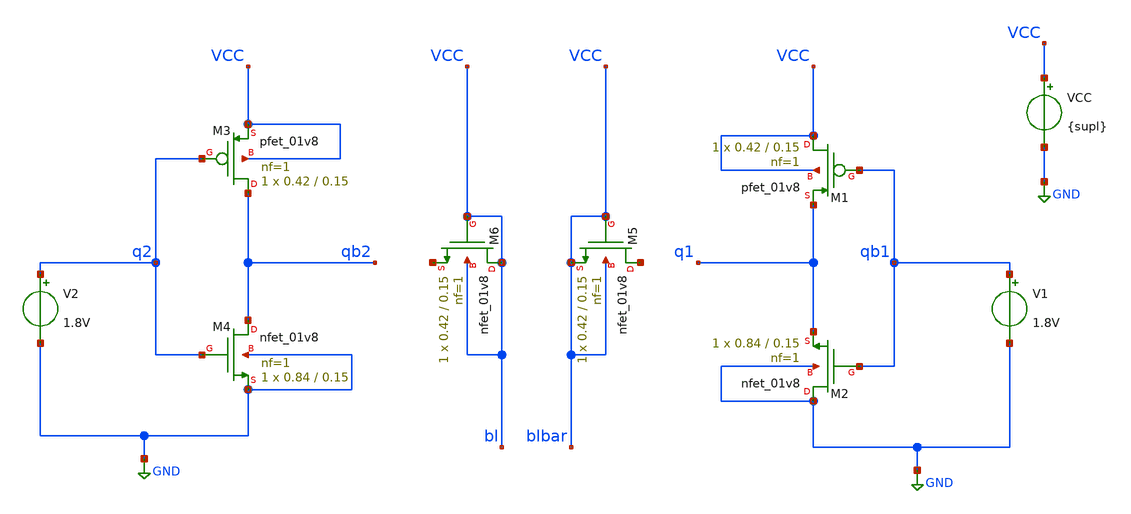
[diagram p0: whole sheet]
** sch_path: Schematics/holdsnm.sch
**.subckt holdsnm
XM1 VCC qb1 q1 VCC sky130_fd_pr__pfet_01v8 L=0.15 W=0.42 nf=1 ad='int((1 + 1)/2) * 0.42 / 1 * 0.29' as='int((1 + 2)/2) * 0.42 / 1 * 0.29'
+ pd='2*int((1 + 1)/2) * (0.42 / 1 + 0.29)' ps='2*int((1 + 2)/2) * (0.42 / 1 + 0.29)' nrd='0.29 / 0.42 '
+ nrs='0.29 / 0.42 ' sa=0 sb=0 sd=0 mult=1 m=1
XM2 GND qb1 q1 GND sky130_fd_pr__nfet_01v8 L=0.15 W=0.84 nf=1 ad='int((1 + 1)/2) * 0.84 / 1 * 0.29' as='int((1 + 2)/2) * 0.84 / 1 * 0.29'
+ pd='2*int((1 + 1)/2) * (0.84 / 1 + 0.29)' ps='2*int((1 + 2)/2) * (0.84 / 1 + 0.29)' nrd='0.29 / 0.84 '
+ nrs='0.29 / 0.84 ' sa=0 sb=0 sd=0 mult=1 m=1
XM3 qb2 q2 VCC VCC sky130_fd_pr__pfet_01v8 L=0.15 W=0.42 nf=1 ad='int((1 + 1)/2) * 0.42 / 1 * 0.29' as='int((1 + 2)/2) * 0.42 / 1 * 0.29'
+ pd='2*int((1 + 1)/2) * (0.42 / 1 + 0.29)' ps='2*int((1 + 2)/2) * (0.42 / 1 + 0.29)' nrd='0.29 / 0.42 '
+ nrs='0.29 / 0.42 ' sa=0 sb=0 sd=0 mult=1 m=1
XM4 qb2 q2 GND GND sky130_fd_pr__nfet_01v8 L=0.15 W=0.84 nf=1 ad='int((1 + 1)/2) * 0.84 / 1 * 0.29' as='int((1 + 2)/2) * 0.84 / 1 * 0.29'
+ pd='2*int((1 + 1)/2) * (0.84 / 1 + 0.29)' ps='2*int((1 + 2)/2) * (0.84 / 1 + 0.29)' nrd='0.29 / 0.84 '
+ nrs='0.29 / 0.84 ' sa=0 sb=0 sd=0 mult=1 m=1
XM5 net1 VCC VCC VCC sky130_fd_pr__nfet_01v8 L=0.15 W=0.42 nf=1 ad='int((1 + 1)/2) * 0.42 / 1 * 0.29'
+ as='int((1 + 2)/2) * 0.42 / 1 * 0.29' pd='2*int((1 + 1)/2) * (0.42 / 1 + 0.29)' ps='2*int((1 + 2)/2) * (0.42 / 1 + 0.29)'
+ nrd='0.29 / 0.42 ' nrs='0.29 / 0.42 ' sa=0 sb=0 sd=0 mult=1 m=1
XM6 VCC VCC net2 VCC sky130_fd_pr__nfet_01v8 L=0.15 W=0.42 nf=1 ad='int((1 + 1)/2) * 0.42 / 1 * 0.29'
+ as='int((1 + 2)/2) * 0.42 / 1 * 0.29' pd='2*int((1 + 1)/2) * (0.42 / 1 + 0.29)' ps='2*int((1 + 2)/2) * (0.42 / 1 + 0.29)'
+ nrd='0.29 / 0.42 ' nrs='0.29 / 0.42 ' sa=0 sb=0 sd=0 mult=1 m=1
V2 q2 GND 1.8V
V1 qb1 GND 1.8V
VCC VCC GND {supl}
**** begin user architecture code

.lib /usr/local/share/pdk/sky130A/libs.tech/ngspice/sky130.lib.spice tt
.param temp=27
.param supl=1.8

.dc V1 0 1.8 0.01 V2 0 1.8 0.01
.control
run
setplot
setplot dc1
plot q1 vs qb1 q2 vs qb2
set filetype=ascii
wrdata /home/scholes33/Projects/PreLayout/Xschem/holdsnm.txt q1 qb1 q2 qb2
.endc
.end


**** end user architecture code
**.ends
.GLOBAL GND
.end
